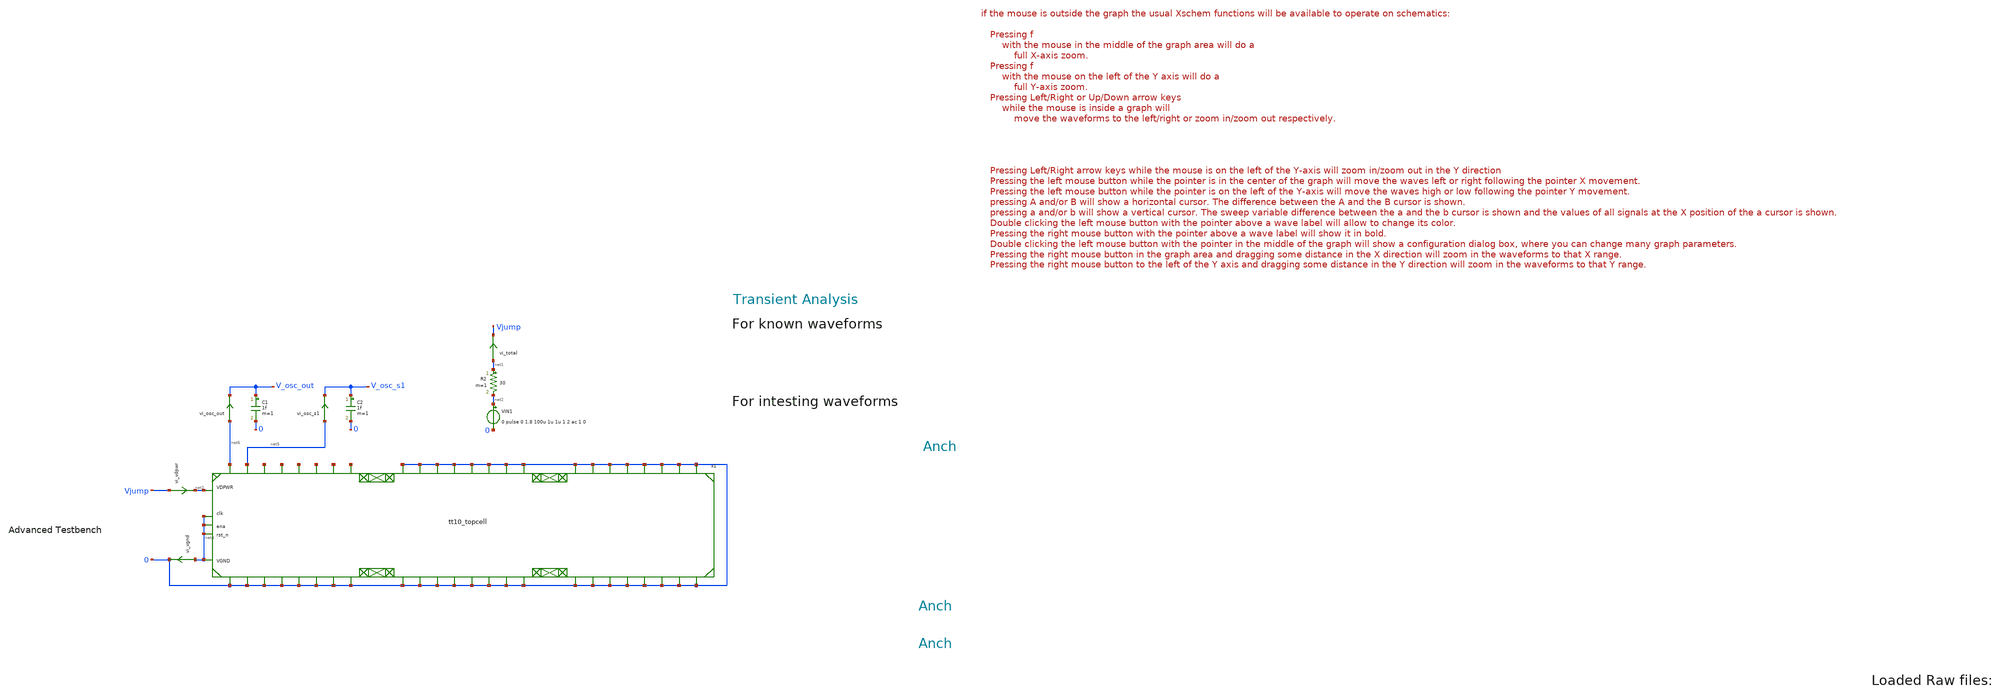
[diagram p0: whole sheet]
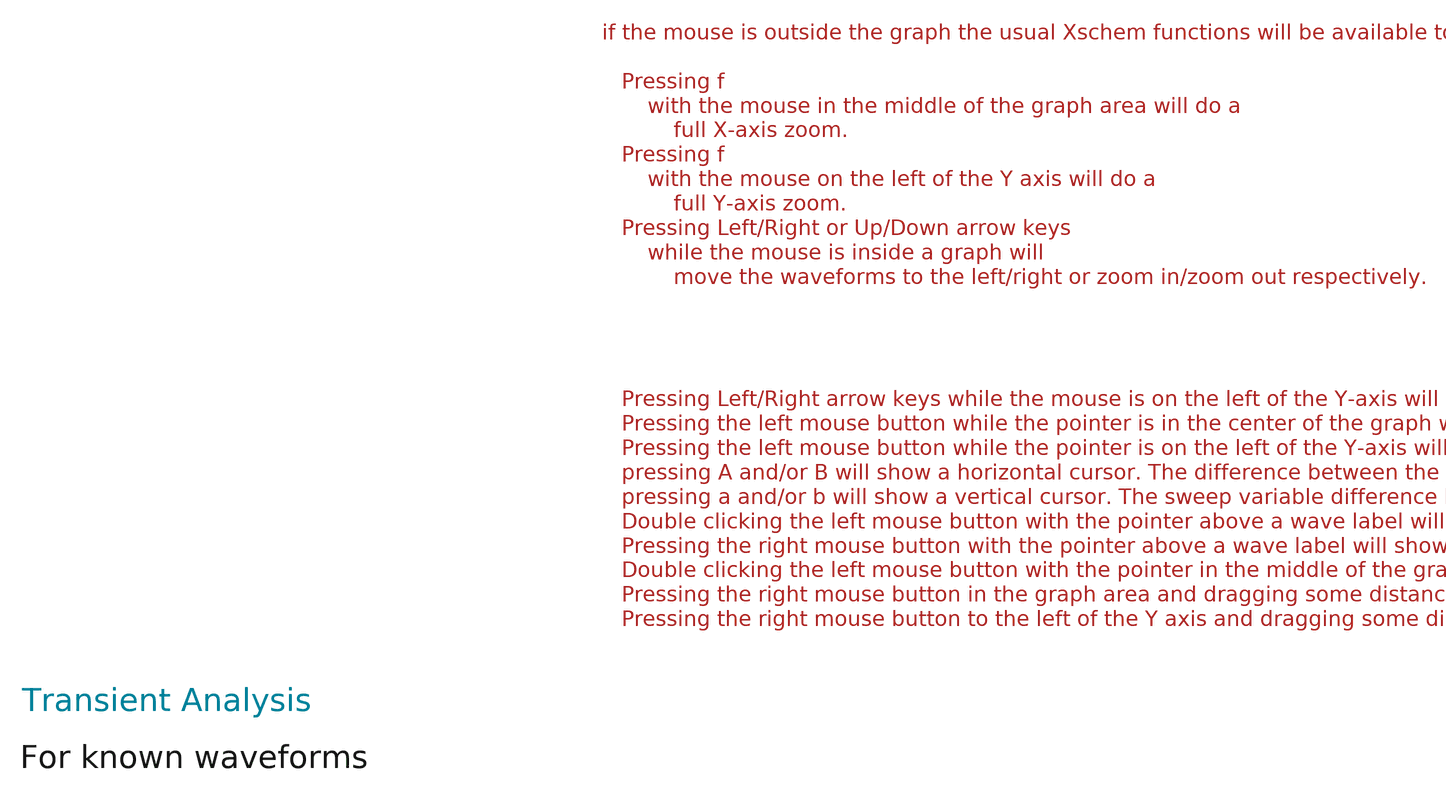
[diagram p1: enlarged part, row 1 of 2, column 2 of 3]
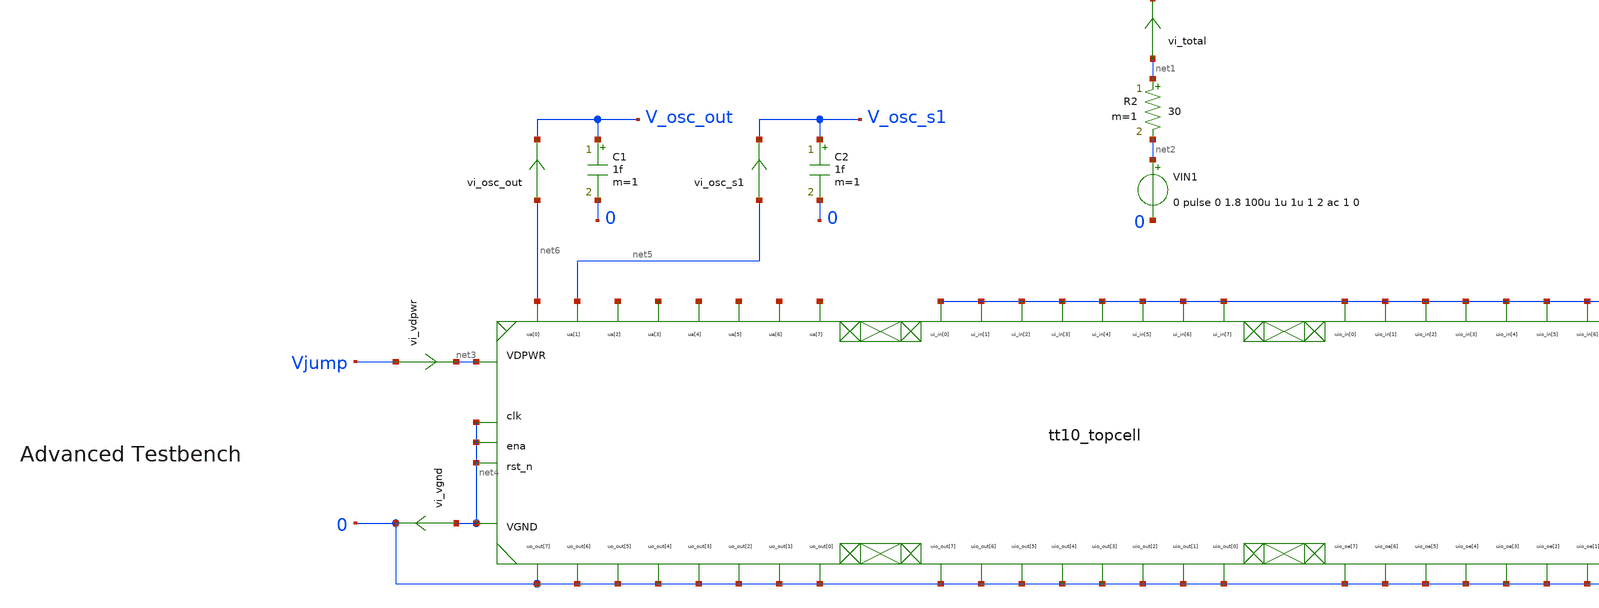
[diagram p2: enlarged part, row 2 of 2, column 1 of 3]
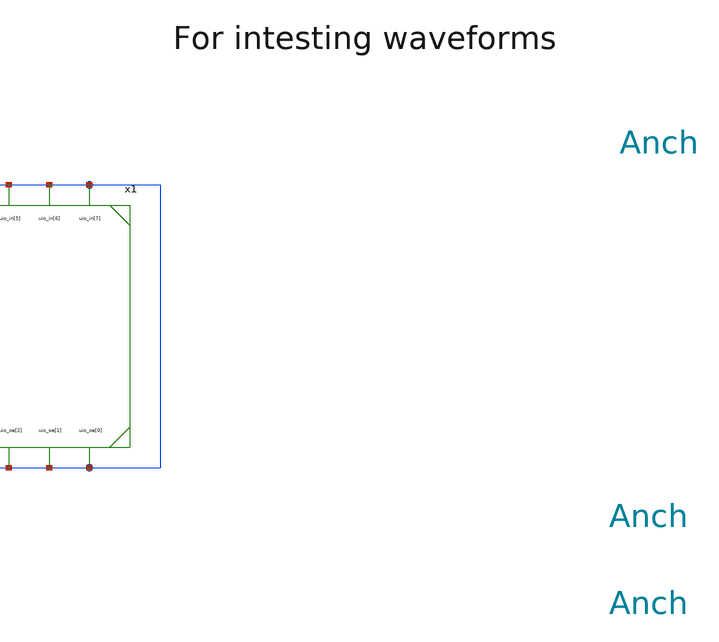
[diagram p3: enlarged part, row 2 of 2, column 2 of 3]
** sch_path: tt10-hdl/tt_um_test_commit/xschem/tt10_topcell_parax_tb.sch
* Copyright (C) 1998-2024 Stefan Frederik Schippers
* This program is free software; you can redistribute it and/or modify
* it under the terms of the GNU General Public License as published by
* the Free Software Foundation; either version 2 of the License, or
* (at your option) any later version.
* This program is distributed in the hope that it will be useful,
* but WITHOUT ANY WARRANTY; without even the implied warranty of
* MERCHANTABILITY or FITNESS FOR A PARTICULAR PURPOSE.  See the
* GNU General Public License for more details.
* You should have received a copy of the GNU General Public License
* along with this program; if not, write to the Free Software
**.subckt tt10_topcell_parax_tb
VIN1 net2 0 0 pulse 0 1.8 100u 1u 1u 1 2 ac 1 0
vi_total net1 Vjump 0
.save i(vi_total)
R2 net1 net2 30 m=1
C1 V_osc_out 0 1f m=1
vi_vdpwr Vjump net3 0
.save i(vi_vdpwr)
vi_vgnd net4 0 0
.save i(vi_vgnd)
x1 net3 net6 net5 net7 net8 net9 net10 net11 net12 0 0 0 0 0 0 0 0 0 0 0 0 0 0 0 0 0 0 0 0 0 0 0 0 0
+ 0 0 0 0 0 0 0 0 0 0 0 0 0 0 0 net4 net4 net4 net4 tt10_topcell
C2 V_osc_s1 0 1f m=1
vi_osc_out net6 V_osc_out 0
.save i(vi_osc_out)
vi_osc_s1 net5 V_osc_s1 0
.save i(vi_osc_s1)
**** begin user architecture code



.temp 30
.param Vdd = 1.8
.param imax = 100e-9


.option savecurrents
.save all
.control
  save all alli
  save

  op
  write osc_51k5Hz_tb.raw
  remzerovec
  set appendwrite

  tran 0.1u 1.5m
  remzerovec
  write osc_51k5Hz_tb.raw





  *quit 0




.endc





** opencircuitdesign pdks install
.lib $::SKYWATER_MODELS/sky130.lib.spice tt


**** end user architecture code
**.ends

* expanding   symbol:  Z_tt10/tt10_topcell.sym # of pins=53
** sym_path: tt10-hdl/tt_um_test_commit/xschem/Z_tt10/tt10_topcell.sym
.include Z_tt10/tt10_topcell_flat.spice
.end
